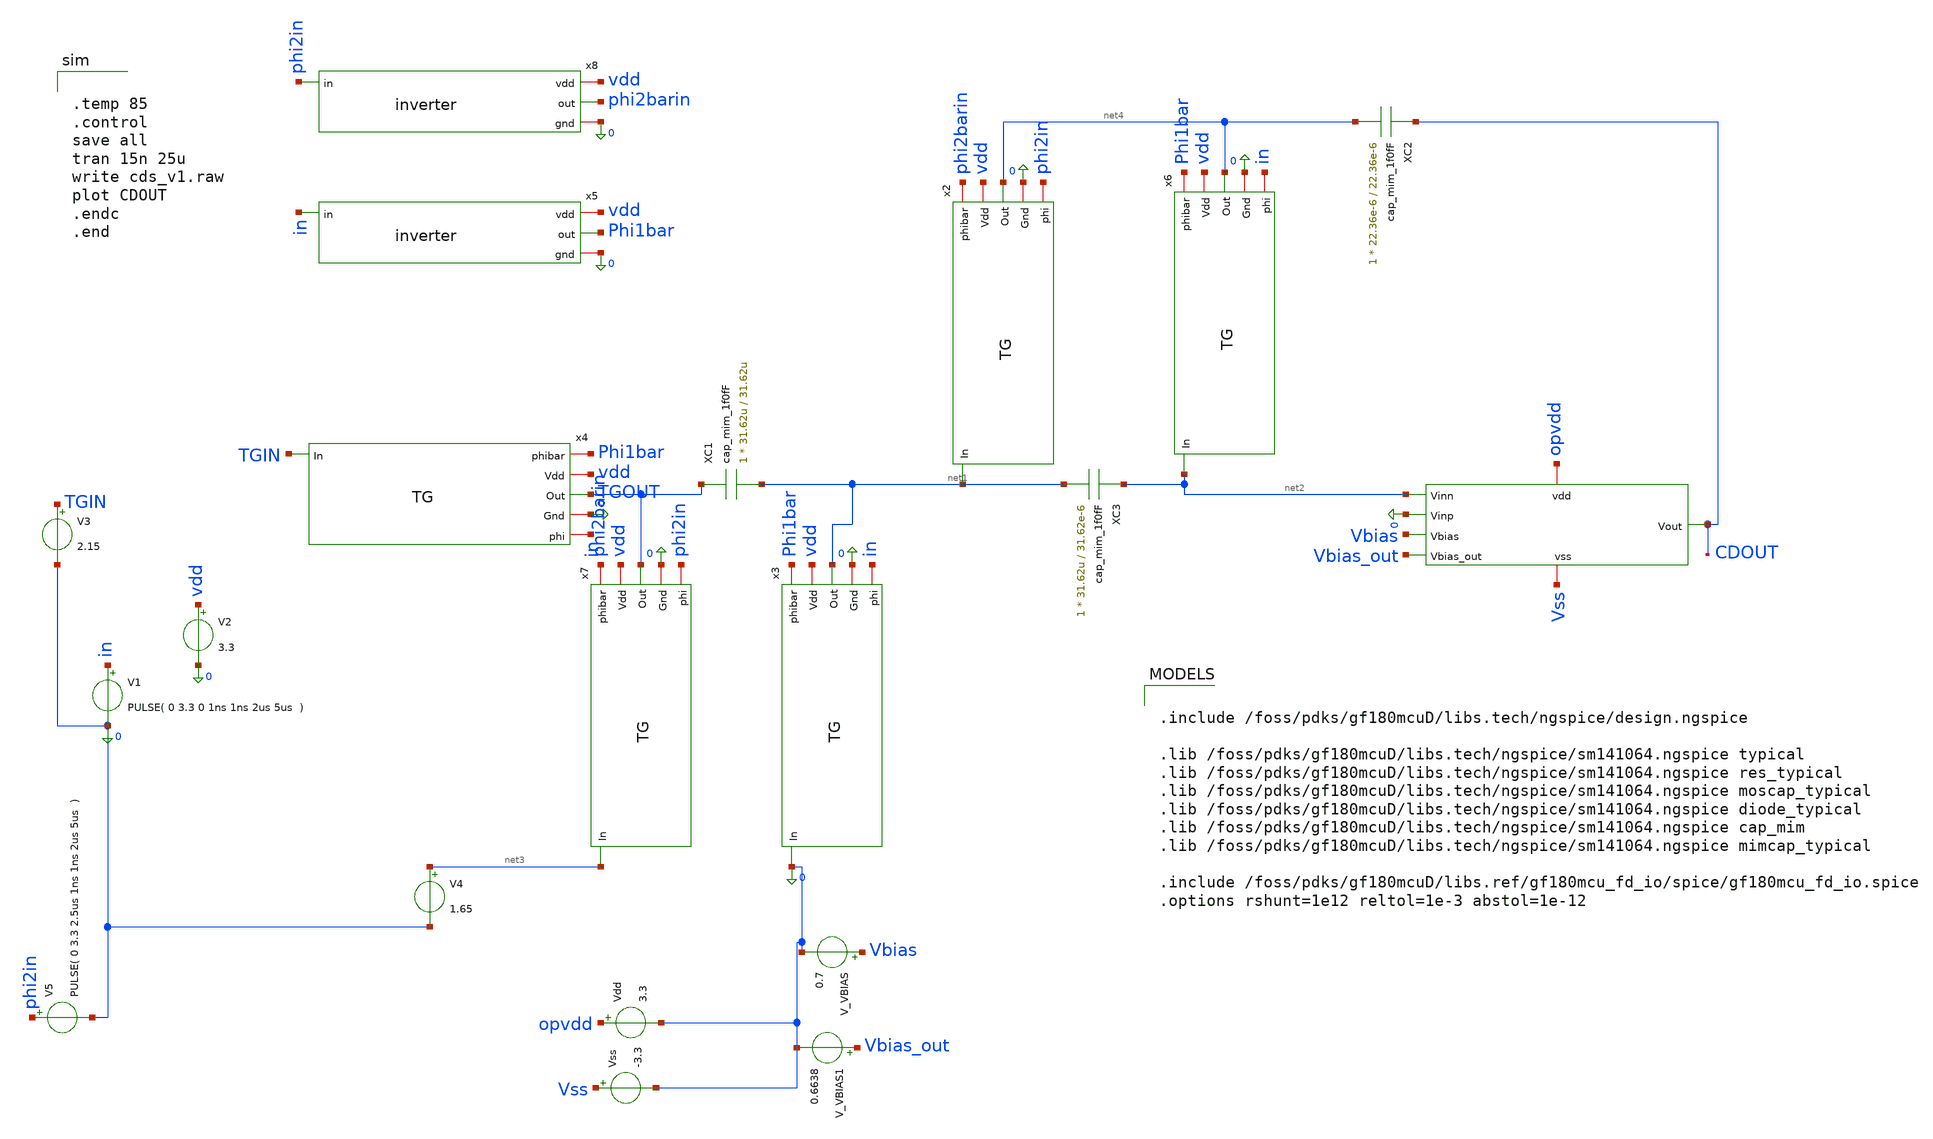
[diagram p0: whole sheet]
** sch_path: xschem/c2v_frontend/cds_v1.sch
**.subckt cds_v1
XC1 TGOUT net1 cap_mim_1f0fF c_width=31.62u c_length=31.62u m=1
XC2 CDOUT net4 cap_mim_1f0fF c_width=22.36e-6 c_length=22.36e-6 m=1
x2 phi2barin vdd net1 net4 0 phi2in TG
x3 Phi1bar vdd 0 net1 0 in TG
x4 Phi1bar vdd TGIN TGOUT 0 in TG
x5 vdd in Phi1bar 0 inverter
V1 in 0 PULSE( 0 3.3 0 1ns 1ns 2us 5us )
V2 vdd 0 3.3
V3 TGIN 0 2.15
x1 CDOUT net2 opvdd 0 Vbias Vss Vbias_out op-amp
x6 Phi1bar vdd net2 net4 0 in TG
XC3 net2 net1 cap_mim_1f0fF c_width=31.62u c_length=31.62e-6 m=1
x7 phi2barin vdd net3 TGOUT 0 phi2in TG
V4 net3 0 1.65
V_VBIAS Vbias 0 0.7
V_VBIAS1 Vbias_out 0 0.6638
Vdd opvdd 0 3.3
Vss Vss 0 -3.3
V5 phi2in 0 PULSE( 0 3.3 2.5us 1ns 1ns 2us 5us )
x8 vdd phi2in phi2barin 0 inverter
**** begin user architecture code


.temp 85
.control
save all
tran 15n 25u
write cds_v1.raw
plot CDOUT
.endc
.end



.include /foss/pdks/gf180mcuD/libs.tech/ngspice/design.ngspice

.lib /foss/pdks/gf180mcuD/libs.tech/ngspice/sm141064.ngspice typical
.lib /foss/pdks/gf180mcuD/libs.tech/ngspice/sm141064.ngspice res_typical
.lib /foss/pdks/gf180mcuD/libs.tech/ngspice/sm141064.ngspice moscap_typical
.lib /foss/pdks/gf180mcuD/libs.tech/ngspice/sm141064.ngspice diode_typical
.lib /foss/pdks/gf180mcuD/libs.tech/ngspice/sm141064.ngspice cap_mim
.lib /foss/pdks/gf180mcuD/libs.tech/ngspice/sm141064.ngspice mimcap_typical

.include /foss/pdks/gf180mcuD/libs.ref/gf180mcu_fd_io/spice/gf180mcu_fd_io.spice
.options rshunt=1e12 reltol=1e-3 abstol=1e-12


**** end user architecture code
**.ends
.end
